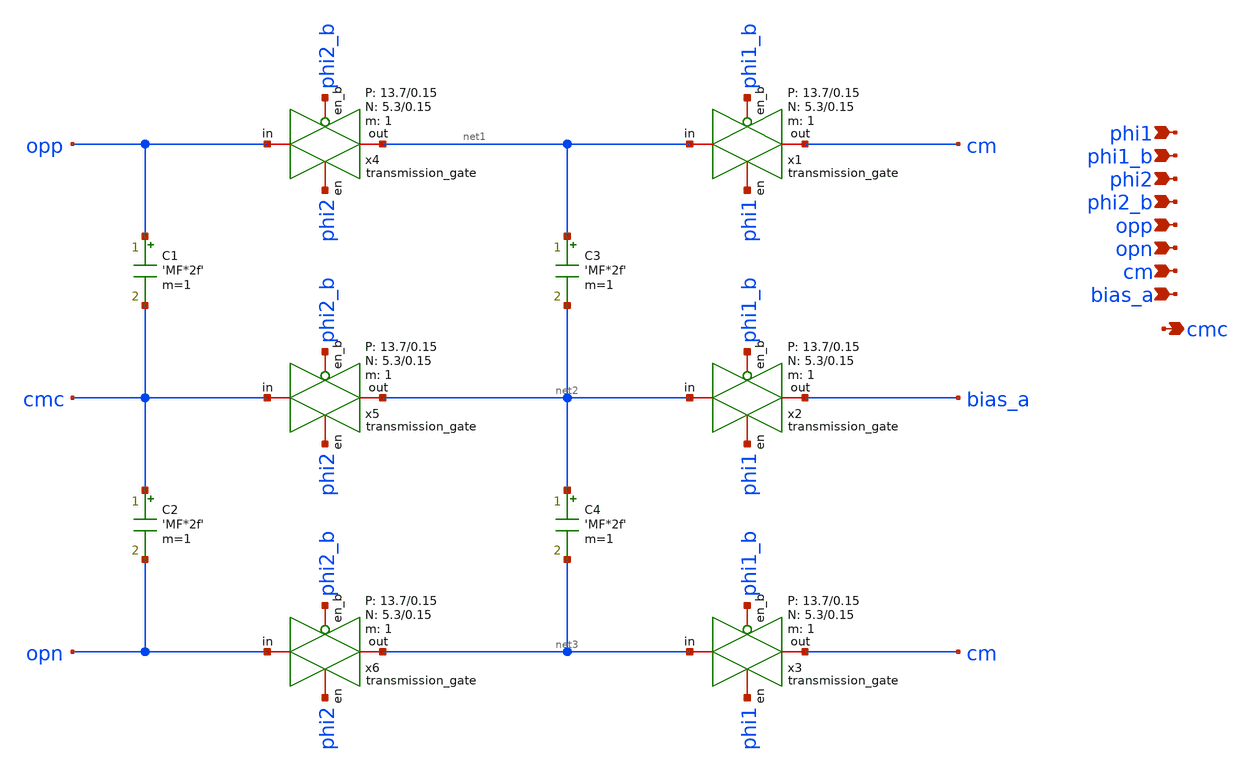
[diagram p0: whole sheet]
** sch_path: design/schematic/ideal_sc_cmfb.sch
**.subckt ideal_sc_cmfb opn cm bias_a opp cmc phi2_b phi2 phi1_b phi1
*.ipin opn
*.ipin cm
*.ipin bias_a
*.ipin opp
*.opin cmc
*.ipin phi2_b
*.ipin phi2
*.ipin phi1_b
*.ipin phi1
x1 net1 cm phi1 phi1_b VDD GND 1 5.3 0.15 13.7 0.15 transmission_gate
x2 net2 bias_a phi1 phi1_b VDD GND 1 5.3 0.15 13.7 0.15 transmission_gate
x3 net3 cm phi1 phi1_b VDD GND 1 5.3 0.15 13.7 0.15 transmission_gate
x4 opp net1 phi2 phi2_b VDD GND 1 5.3 0.15 13.7 0.15 transmission_gate
x5 cmc net2 phi2 phi2_b VDD GND 1 5.3 0.15 13.7 0.15 transmission_gate
x6 opn net3 phi2 phi2_b VDD GND 1 5.3 0.15 13.7 0.15 transmission_gate
C1 opp cmc 'MF*2f' m=1
C2 cmc opn 'MF*2f' m=1
C3 net1 net2 'MF*2f' m=1
C4 net2 net3 'MF*2f' m=1
**.ends

* expanding   symbol:  transmission_gate.sym # of pins=4
** sym_path: design/schematic/transmission_gate.sym
** sch_path: design/schematic/transmission_gate.sch
.subckt transmission_gate in out en en_b VDD VSS N W_N L_N W_P L_P    N=1 W_N=5.3 L_N=0.15 W_P=13.7
+ L_P=0.15
*.iopin in
*.iopin out
*.ipin en
*.ipin en_b
XM1 out en in VSS sky130_fd_pr__nfet_01v8 L=L_N W=W_N nf=1 ad='int((nf+1)/2) * W/nf * 0.29' as='int((nf+2)/2) * W/nf * 0.29'
+ pd='2*int((nf+1)/2) * (W/nf + 0.29)' ps='2*int((nf+2)/2) * (W/nf + 0.29)' nrd='0.29 / W' nrs='0.29 / W'
+ sa=0 sb=0 sd=0 mult=N m=N
XM2 out en_b in VDD sky130_fd_pr__pfet_01v8 L=L_P W=W_P nf=1 ad='int((nf+1)/2) * W/nf * 0.29' as='int((nf+2)/2) * W/nf * 0.29'
+ pd='2*int((nf+1)/2) * (W/nf + 0.29)' ps='2*int((nf+2)/2) * (W/nf + 0.29)' nrd='0.29 / W' nrs='0.29 / W'
+ sa=0 sb=0 sd=0 mult=N m=N
.ends

.end
